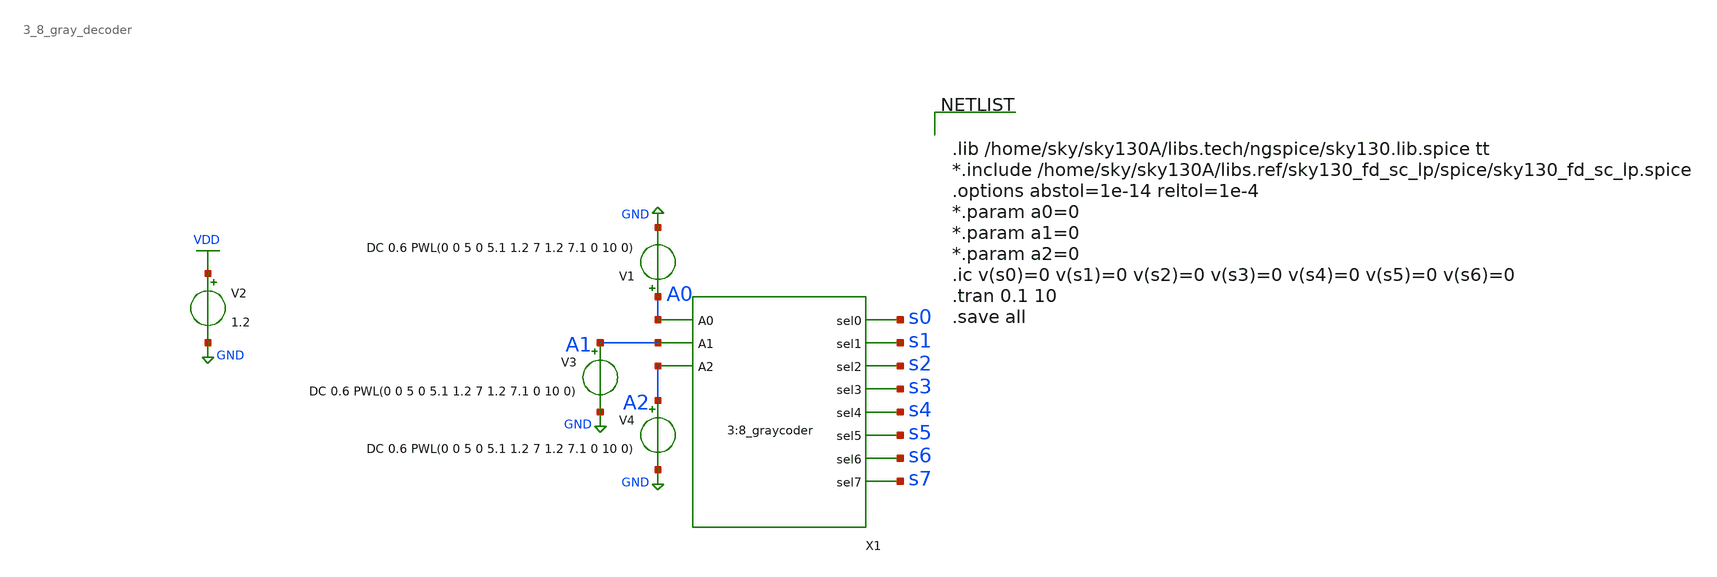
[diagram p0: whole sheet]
** sch_path: xschem/decoder/3_8_gray_decoder_tb.sch
**.subckt 3_8_gray_decoder_tb
X1 A0 A1 A2 s0 s1 s2 s3 s4 s5 s6 s7 3_8_gray_decoder
V1 A0 GND DC 0.6 PWL(0 0 5 0 5.1 1.2 7 1.2 7.1 0 10 0)
V2 VDD GND 1.2
V3 A1 GND DC 0.6 PWL(0 0 5 0 5.1 1.2 7 1.2 7.1 0 10 0)
V4 A2 GND DC 0.6 PWL(0 0 5 0 5.1 1.2 7 1.2 7.1 0 10 0)
**** begin user architecture code


.lib /home/sky/sky130A/libs.tech/ngspice/sky130.lib.spice tt
*.include /home/sky/sky130A/libs.ref/sky130_fd_sc_lp/spice/sky130_fd_sc_lp.spice
.options abstol=1e-14 reltol=1e-4
*.param a0=0
*.param a1=0
*.param a2=0
.ic v(s0)=0 v(s1)=0 v(s2)=0 v(s3)=0 v(s4)=0 v(s5)=0 v(s6)=0
.tran 0.1 10
.save all


**** end user architecture code
**.ends
.GLOBAL GND
.GLOBAL VDD
.end
